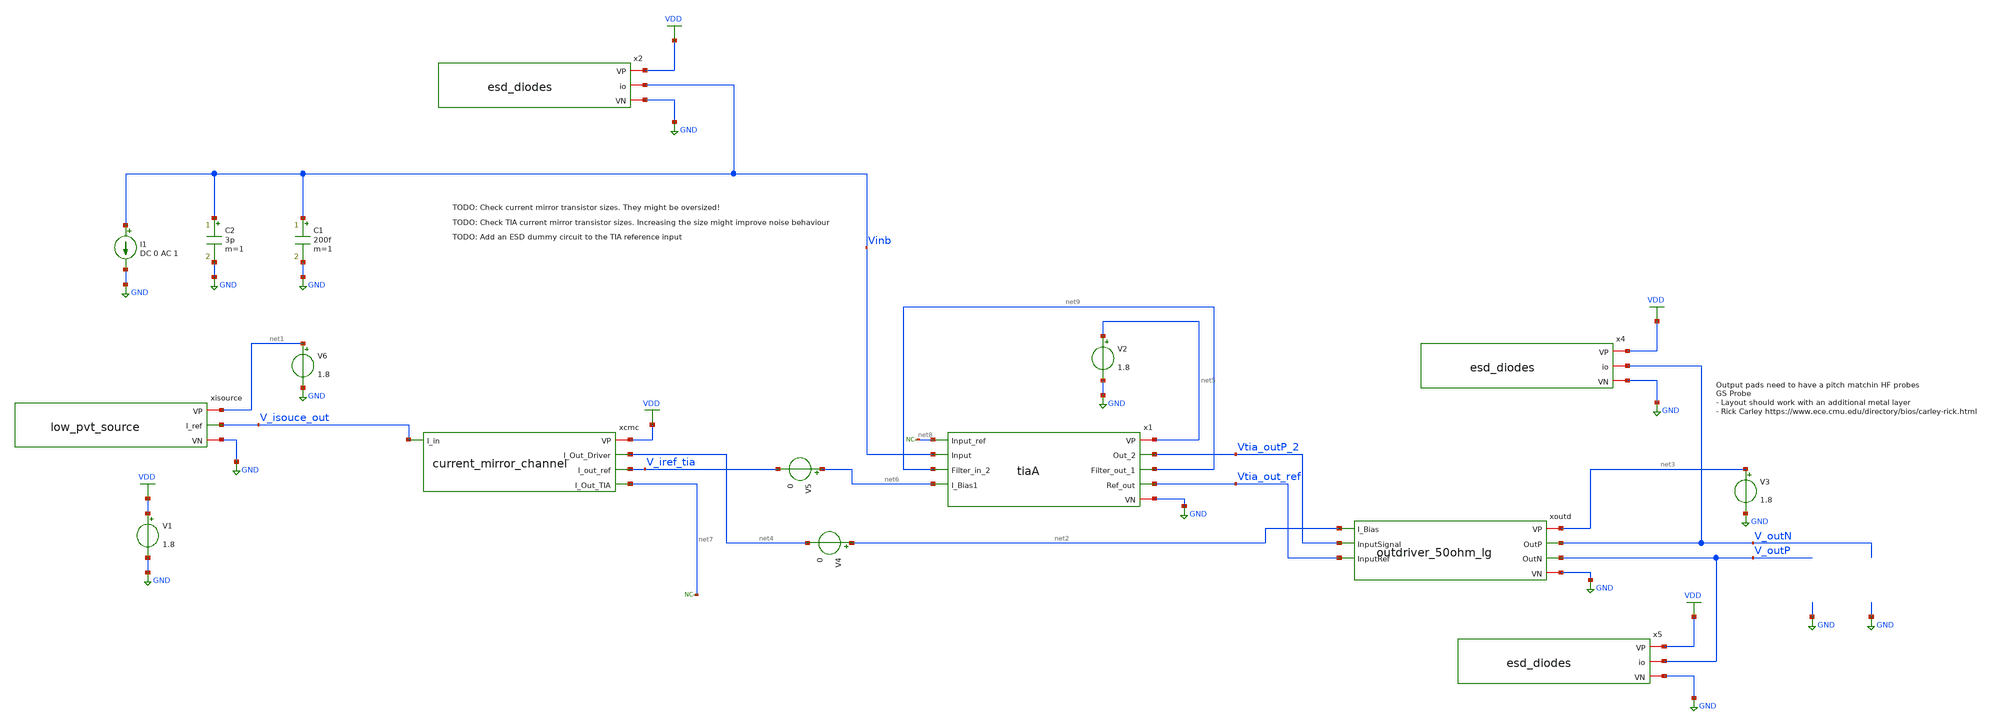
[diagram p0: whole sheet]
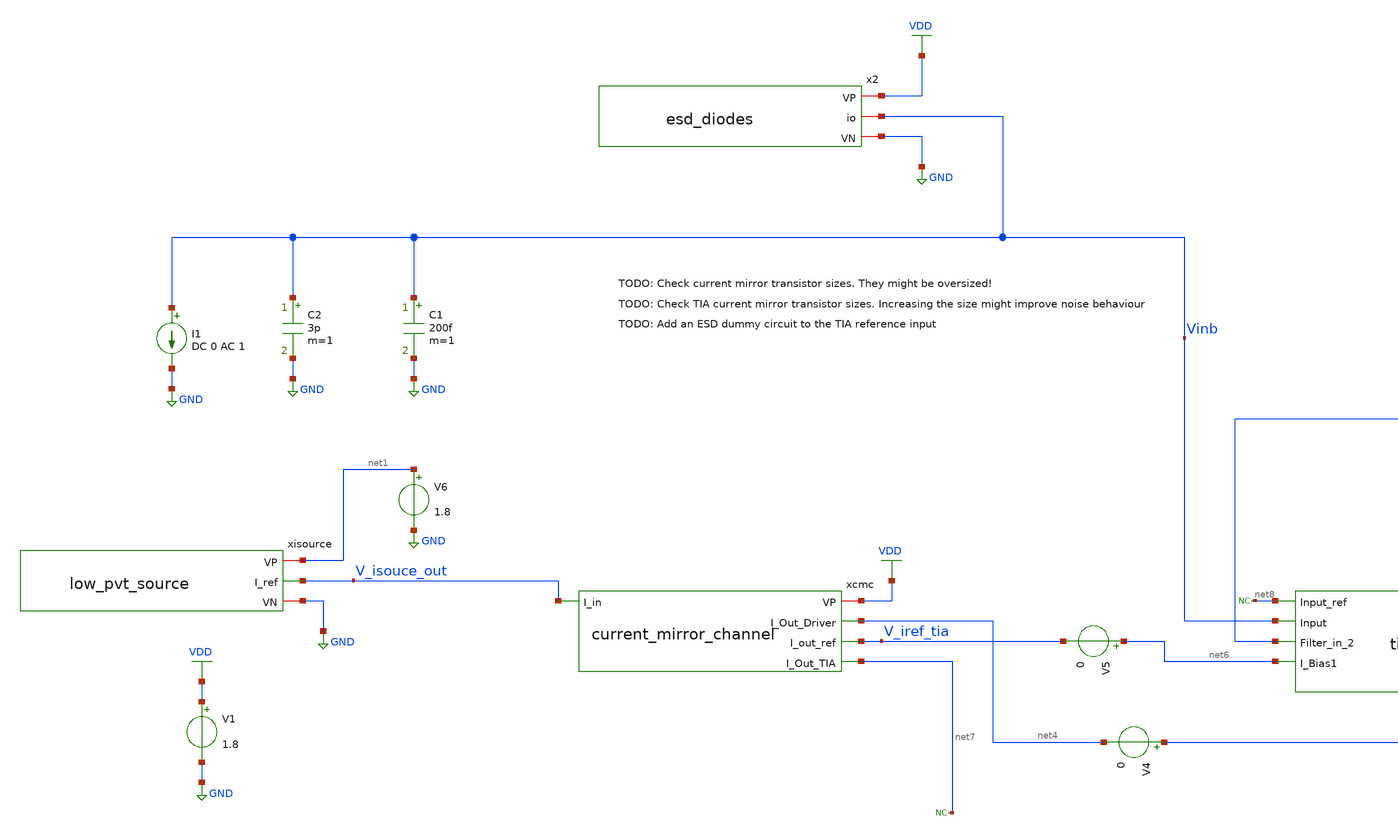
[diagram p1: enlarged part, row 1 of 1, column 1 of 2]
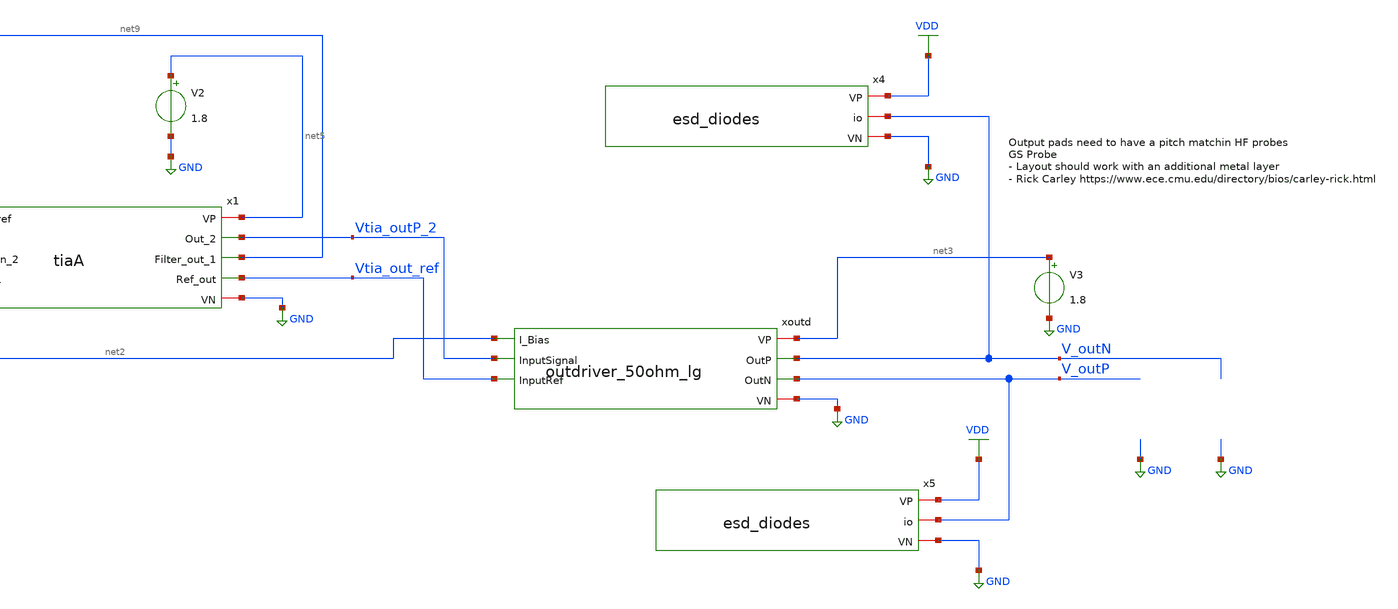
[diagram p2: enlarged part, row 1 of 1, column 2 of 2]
** sch_path: xschem/test/test_tia_integration.sch
**.subckt test_tia_integration
xisource net1 V_isouce_out GND low_pvt_source
V1 VDD GND 1.8
I1 Vinb GND DC 0 AC 1
C1 Vinb GND 200f m=1
C2 Vinb GND 3p m=1
xcmc VDD V_isouce_out net4 V_iref_tia net7 current_mirror_channel
x4 VDD V_outN GND esd_diodes
x5 VDD V_outP GND esd_diodes
x2 VDD Vinb GND esd_diodes
V2 net5 GND 1.8
V3 net3 GND 1.8
V4 net2 net4 0
V5 net6 V_iref_tia 0
V6 net1 GND 1.8
* noconn #net8
* noconn #net7
x1 net5 Vtia_outP_2 net9 net8 Vinb net9 Vtia_out_ref net6 GND tiaA
xoutd net3 V_outN V_outP net2 Vtia_outP_2 Vtia_out_ref GND outdriver_50ohm_lg
**** begin user architecture code


*.options savecurrents
.option warn=1
.option temp=20
.control
set wr_vecnames
set wr_singlescale
set hcopydevtype=svg
** TIA



* save @m.xtia.xm1.msky130_fd_pr__nfet_01v8_lvt[gm]
* save @m.xtia.xm7.msky130_fd_pr__nfet_01v8_lvt[gm]
* save @m.xtia.xm17.msky130_fd_pr__nfet_01v8_lvt[gm]
* save @m.xtia.xm16.msky130_fd_pr__pfet_01v8[gm]
* save @m.xtia.xm8.msky130_fd_pr__pfet_01v8[gm]

* save @m.xtia.xm7.msky130_fd_pr__nfet_01v8_lvt[gm]
* save @m.xtia.xm8.msky130_fd_pr__pfet_01v8[gm]
save all
op
run
write test_tia_integration.raw
reset
save all
ac dec 10 10 1T
plot vdb(Vtia_outP_2)
plot v(Vinb)
plot phase(Vinb)/pi*180 phase(Vtia_outP_1)/pi*180 phase(Vtia_outP_2)/pi*180

*plot phase(Vinb)/pi*180 phase(Vtia_outP_1-Vinb)/pi*180


plot db(v(xoutd.V_da2_P)-v(xoutd.V_da2_N)) - db(v(Vtia_outP_2)-v(Vtia_out_ref))
plot db(v(xoutd.V_da3_P)-v(xoutd.V_da3_N)) - db(v(xoutd.V_da2_P)-v(xoutd.V_da2_N))
plot db(v(xoutd.V_da3_P)-v(xoutd.V_da3_N)) - db(v(Vtia_outP_2)-v(Vtia_out_ref))



*plot db(v(xoutd.V_da2_P)-v(xoutd.V_da2_N)) - db(v(xoutd.V_da1_P)-v(xoutd.V_da1_N))
plot db(v(V_outP)-v(V_outN)) - db(v(xoutd.V_da3_P)-v(xoutd.V_da3_N))


*plot db(v(xoutd.v_da1_P)-v(xoutd.v_da1_N))

plot db(v(V_outP) - v(V_outN))

* tran 1p 100n
* plot v(Vinb)

meas ac gain FIND vdb(vtia_outp_1) AT=10MEG
meas ac max_gain max vdb(vtia_outp_1) from=1MEG to=100G
meas ac min_gain min vdb(vtia_outp_1) from=1MEG to=100MEG
let bw_gain=gain-3
meas ac bandwidth when vdb(vtia_outp_1)=bw_gain fall = LAST
wrdata result_ac_tia.csv gain max_gain min_gain bandwidth


noise v(vtia_outp_2) i1 dec 10 10 2G
print all
* wrdata result_noise.csv inoise_total onoise_total
setplot noise1
plot inoise_spectrum
plot onoise_spectrum
* hardcopy tia_rgc_inoise_spectrum.svg inoise_spectrum
* hardcopy tia_rgc_onoise_spectrum.svg onoise_spectrum
* plot log(inoise_spectrum)
* write noise_tia2.raw

noise v(vtia_outp_2, vtia_out_ref) i1 dec 10 1MEG 2G
print all
* wrdata result_noise.csv inoise_total onoise_total
setplot noise3
plot inoise_spectrum
plot onoise_spectrum
* hardcopy tia_rgc_inoise_spectrum_zoom.svg inoise_spectrum
* hardcopy tia_rgc_onoise_spectrum_zoom.svg onoise_spectrum
* plot log(inoise_spectrum)
* write noise_tia2.raw

noise v(v_outp,v_outn) i1 dec 10 1MEG 2G
print all
setplot noise5
plot inoise_spectrum
plot onoise_spectrum

noise v(v_outp,v_outn) i1 dec 10 10 2G
print all
setplot noise7
plot inoise_spectrum
plot onoise_spectrum


.endc




* .include ../../tia.spice
* .include ../../filter_diff.spice
* .include ../../cmm_sense3.spice

.include tiaA.spice
.include current_mirror_channel.spice
.include low_pvt_source.spice
.include outdriver.spice
.include outdriver_50ohm.spice
.include outdriver_50ohm_lg.spice
.include esd_diodes.spice



* .lib $::SKYWATER_MODELS/sky130.lib.spice #model#
* .lib $::SKYWATER_MODELS/sky130.lib.spice sf
.lib $::SKYWATER_MODELS/sky130.lib.spice.tt.red tt

**** end user architecture code
**.ends

* expanding   symbol:  ../bias/low_pvt_source.sym # of pins=3
** sym_path: ../bias/low_pvt_source.sym
** sch_path: ../bias/low_pvt_source.sch
.subckt low_pvt_source VP I_ref VN
*.iopin VP
*.opin I_ref
*.iopin VN
XM1 VM1D VM8D VP VP sky130_fd_pr__pfet_01v8 L=1 W=4 nf=1 ad='int((nf+1)/2) * W/nf * 0.29' as='int((nf+2)/2) * W/nf * 0.29'
+ pd='2*int((nf+1)/2) * (W/nf + 0.29)' ps='2*int((nf+2)/2) * (W/nf + 0.29)' nrd='0.29 / W' nrs='0.29 / W'
+ sa=0 sb=0 sd=0 mult=10 m=10
XM2 VM2D VM2D VN VN sky130_fd_pr__nfet_01v8 L=6 W=4 nf=1 ad='int((nf+1)/2) * W/nf * 0.29' as='int((nf+2)/2) * W/nf * 0.29'
+ pd='2*int((nf+1)/2) * (W/nf + 0.29)' ps='2*int((nf+2)/2) * (W/nf + 0.29)' nrd='0.29 / W' nrs='0.29 / W'
+ sa=0 sb=0 sd=0 mult=30 m=30
XM5 VM9D VM8D VM1D VP sky130_fd_pr__pfet_01v8 L=0.2 W=4 nf=1 ad='int((nf+1)/2) * W/nf * 0.29' as='int((nf+2)/2) * W/nf * 0.29'
+ pd='2*int((nf+1)/2) * (W/nf + 0.29)' ps='2*int((nf+2)/2) * (W/nf + 0.29)' nrd='0.29 / W' nrs='0.29 / W'
+ sa=0 sb=0 sd=0 mult=2 m=2
XM11 VM11D VM2D VM12D VN sky130_fd_pr__nfet_01v8 L=6 W=4 nf=1 ad='int((nf+1)/2) * W/nf * 0.29' as='int((nf+2)/2) * W/nf * 0.29'
+ pd='2*int((nf+1)/2) * (W/nf + 0.29)' ps='2*int((nf+2)/2) * (W/nf + 0.29)' nrd='0.29 / W' nrs='0.29 / W'
+ sa=0 sb=0 sd=0 mult=65 m=65
XM12 VM12D VM12G VN VN sky130_fd_pr__nfet_01v8 L=6 W=4 nf=1 ad='int((nf+1)/2) * W/nf * 0.29' as='int((nf+2)/2) * W/nf * 0.29'
+ pd='2*int((nf+1)/2) * (W/nf + 0.29)' ps='2*int((nf+2)/2) * (W/nf + 0.29)' nrd='0.29 / W' nrs='0.29 / W'
+ sa=0 sb=0 sd=0 mult=2 m=2
XM14 VM14D VM12G VN VN sky130_fd_pr__nfet_01v8 L=6 W=4 nf=1 ad='int((nf+1)/2) * W/nf * 0.29' as='int((nf+2)/2) * W/nf * 0.29'
+ pd='2*int((nf+1)/2) * (W/nf + 0.29)' ps='2*int((nf+2)/2) * (W/nf + 0.29)' nrd='0.29 / W' nrs='0.29 / W'
+ sa=0 sb=0 sd=0 mult=2 m=2
XM16 VM16D VM8D VP VP sky130_fd_pr__pfet_01v8 L=1 W=4 nf=1 ad='int((nf+1)/2) * W/nf * 0.29' as='int((nf+2)/2) * W/nf * 0.29'
+ pd='2*int((nf+1)/2) * (W/nf + 0.29)' ps='2*int((nf+2)/2) * (W/nf + 0.29)' nrd='0.29 / W' nrs='0.29 / W'
+ sa=0 sb=0 sd=0 mult=10 m=10
XM17 VM8D VM8D VM16D VP sky130_fd_pr__pfet_01v8 L=0.2 W=4 nf=1 ad='int((nf+1)/2) * W/nf * 0.29' as='int((nf+2)/2) * W/nf * 0.29'
+ pd='2*int((nf+1)/2) * (W/nf + 0.29)' ps='2*int((nf+2)/2) * (W/nf + 0.29)' nrd='0.29 / W' nrs='0.29 / W'
+ sa=0 sb=0 sd=0 mult=2 m=2
XM18 VM18D VM8D VP VP sky130_fd_pr__pfet_01v8 L=1 W=4 nf=1 ad='int((nf+1)/2) * W/nf * 0.29' as='int((nf+2)/2) * W/nf * 0.29'
+ pd='2*int((nf+1)/2) * (W/nf + 0.29)' ps='2*int((nf+2)/2) * (W/nf + 0.29)' nrd='0.29 / W' nrs='0.29 / W'
+ sa=0 sb=0 sd=0 mult=10*3*2 m=10*3*2
XM19 VM14D VM8D VM18D VP sky130_fd_pr__pfet_01v8 L=0.2 W=4 nf=1 ad='int((nf+1)/2) * W/nf * 0.29' as='int((nf+2)/2) * W/nf * 0.29'
+ pd='2*int((nf+1)/2) * (W/nf + 0.29)' ps='2*int((nf+2)/2) * (W/nf + 0.29)' nrd='0.29 / W' nrs='0.29 / W'
+ sa=0 sb=0 sd=0 mult=2*3*2 m=2*3*2
XM20 VM20D VM8D VP VP sky130_fd_pr__pfet_01v8 L=1 W=4 nf=1 ad='int((nf+1)/2) * W/nf * 0.29' as='int((nf+2)/2) * W/nf * 0.29'
+ pd='2*int((nf+1)/2) * (W/nf + 0.29)' ps='2*int((nf+2)/2) * (W/nf + 0.29)' nrd='0.29 / W' nrs='0.29 / W'
+ sa=0 sb=0 sd=0 mult=10*1*1 m=10*1*1
XM21 VM22D VM8D VM20D VP sky130_fd_pr__pfet_01v8 L=0.2 W=4 nf=1 ad='int((nf+1)/2) * W/nf * 0.29' as='int((nf+2)/2) * W/nf * 0.29'
+ pd='2*int((nf+1)/2) * (W/nf + 0.29)' ps='2*int((nf+2)/2) * (W/nf + 0.29)' nrd='0.29 / W' nrs='0.29 / W'
+ sa=0 sb=0 sd=0 mult=2*1*1 m=2*1*1
XM22 VM22D VM4S VM3D VN sky130_fd_pr__nfet_01v8 L=6 W=4 nf=1 ad='int((nf+1)/2) * W/nf * 0.29' as='int((nf+2)/2) * W/nf * 0.29'
+ pd='2*int((nf+1)/2) * (W/nf + 0.29)' ps='2*int((nf+2)/2) * (W/nf + 0.29)' nrd='0.29 / W' nrs='0.29 / W'
+ sa=0 sb=0 sd=0 mult=20 m=20
XM3 VM3D VM3G VN VN sky130_fd_pr__nfet_01v8 L=6 W=4 nf=1 ad='int((nf+1)/2) * W/nf * 0.29' as='int((nf+2)/2) * W/nf * 0.29'
+ pd='2*int((nf+1)/2) * (W/nf + 0.29)' ps='2*int((nf+2)/2) * (W/nf + 0.29)' nrd='0.29 / W' nrs='0.29 / W'
+ sa=0 sb=0 sd=0 mult=4 m=4
XM13 VP VM14D VM12G VM12G sky130_fd_pr__nfet_01v8_lvt L=0.15 W=4 nf=1 ad='int((nf+1)/2) * W/nf * 0.29'
+ as='int((nf+2)/2) * W/nf * 0.29' pd='2*int((nf+1)/2) * (W/nf + 0.29)' ps='2*int((nf+2)/2) * (W/nf + 0.29)'
+ nrd='0.29 / W' nrs='0.29 / W' sa=0 sb=0 sd=0 mult=20 m=20
XM4 I_ref VM22D VM4S VN sky130_fd_pr__nfet_01v8_lvt L=0.15 W=4 nf=1 ad='int((nf+1)/2) * W/nf * 0.29'
+ as='int((nf+2)/2) * W/nf * 0.29' pd='2*int((nf+1)/2) * (W/nf + 0.29)' ps='2*int((nf+2)/2) * (W/nf + 0.29)'
+ nrd='0.29 / W' nrs='0.29 / W' sa=0 sb=0 sd=0 mult=20 m=20
XM48 VM50D VM11D VP VP sky130_fd_pr__pfet_01v8 L=2 W=0.5 nf=1 ad='int((nf+1)/2) * W/nf * 0.29' as='int((nf+2)/2) * W/nf * 0.29'
+ pd='2*int((nf+1)/2) * (W/nf + 0.29)' ps='2*int((nf+2)/2) * (W/nf + 0.29)' nrd='0.29 / W' nrs='0.29 / W'
+ sa=0 sb=0 sd=0 mult=1 m=1
XM50 VM50D VM11D VN VN sky130_fd_pr__nfet_01v8_lvt L=0.2 W=4 nf=1 ad='int((nf+1)/2) * W/nf * 0.29' as='int((nf+2)/2) * W/nf * 0.29'
+ pd='2*int((nf+1)/2) * (W/nf + 0.29)' ps='2*int((nf+2)/2) * (W/nf + 0.29)' nrd='0.29 / W' nrs='0.29 / W'
+ sa=0 sb=0 sd=0 mult=10 m=10
XC3 VP VM8D sky130_fd_pr__cap_mim_m3_1 W=20 L=20 MF=1 m=1
XM8 VM8D VM9D VM11D VM11D sky130_fd_pr__nfet_01v8_lvt L=1 W=4 nf=1 ad='int((nf+1)/2) * W/nf * 0.29' as='int((nf+2)/2) * W/nf * 0.29'
+ pd='2*int((nf+1)/2) * (W/nf + 0.29)' ps='2*int((nf+2)/2) * (W/nf + 0.29)' nrd='0.29 / W' nrs='0.29 / W'
+ sa=0 sb=0 sd=0 mult=20 m=20
XM9 VM9D VM9D VM2D VM2D sky130_fd_pr__nfet_01v8_lvt L=1 W=4 nf=1 ad='int((nf+1)/2) * W/nf * 0.29' as='int((nf+2)/2) * W/nf * 0.29'
+ pd='2*int((nf+1)/2) * (W/nf + 0.29)' ps='2*int((nf+2)/2) * (W/nf + 0.29)' nrd='0.29 / W' nrs='0.29 / W'
+ sa=0 sb=0 sd=0 mult=20 m=20
XM10 VM8D VM50D VN VN sky130_fd_pr__nfet_01v8 L=2 W=0.5 nf=1 ad='int((nf+1)/2) * W/nf * 0.29' as='int((nf+2)/2) * W/nf * 0.29'
+ pd='2*int((nf+1)/2) * (W/nf + 0.29)' ps='2*int((nf+2)/2) * (W/nf + 0.29)' nrd='0.29 / W' nrs='0.29 / W'
+ sa=0 sb=0 sd=0 mult=1 m=1
XR7 net3 VM4S VN sky130_fd_pr__res_xhigh_po_1p41 L=10 mult=1 m=1
XR3 net4 net3 VN sky130_fd_pr__res_xhigh_po_1p41 L=10 mult=1 m=1
XR4 net2 net4 VN sky130_fd_pr__res_xhigh_po_1p41 L=10 mult=1 m=1
XR5 net1 net2 VN sky130_fd_pr__res_xhigh_po_1p41 L=10 mult=1 m=1
XR6 VN net1 VN sky130_fd_pr__res_xhigh_po_1p41 L=10 mult=1 m=1
XR8 net5 VM12G VN sky130_fd_pr__res_xhigh_po_1p41 L=10 mult=1 m=1
XR1 net5 VM3G VN sky130_fd_pr__res_xhigh_po_1p41 L=10 mult=1 m=1
XR2 net7 net6 VN sky130_fd_pr__res_xhigh_po_1p41 L=10 mult=1 m=1
XR9 VN net6 VN sky130_fd_pr__res_xhigh_po_1p41 L=10 mult=1 m=1
XR10 net11 net7 VN sky130_fd_pr__res_xhigh_po_1p41 L=10 mult=1 m=1
XR11 net12 net11 VN sky130_fd_pr__res_xhigh_po_1p41 L=10 mult=1 m=1
XR12 net8 net12 VN sky130_fd_pr__res_xhigh_po_1p41 L=10 mult=1 m=1
XR13 net10 VM3G VN sky130_fd_pr__res_xhigh_po_1p41 L=10 mult=1 m=1
XR14 net9 net10 VN sky130_fd_pr__res_xhigh_po_1p41 L=10 mult=1 m=1
XR15 net8 net9 VN sky130_fd_pr__res_xhigh_po_1p41 L=10 mult=1 m=1
XC2 VP VN sky130_fd_pr__cap_mim_m3_1 W=25 L=30 MF=1 m=1
XC1 VP VN sky130_fd_pr__cap_mim_m3_1 W=25 L=30 MF=1 m=1
.ends


* expanding   symbol:  ../bias/current_mirror_channel.sym # of pins=5
** sym_path: xschem/bias/current_mirror_channel.sym
** sch_path: xschem/bias/current_mirror_channel.sch
.subckt current_mirror_channel VP I_in I_Out_Driver I_out_ref I_Out_TIA
*.ipin I_in
*.iopin VP
*.opin I_Out_TIA
*.opin I_Out_Driver
*.opin I_out_ref
XM13 VM13D I_in VP VP sky130_fd_pr__pfet_01v8 L=1 W=2 nf=1 ad='int((nf+1)/2) * W/nf * 0.29' as='int((nf+2)/2) * W/nf * 0.29'
+ pd='2*int((nf+1)/2) * (W/nf + 0.29)' ps='2*int((nf+2)/2) * (W/nf + 0.29)' nrd='0.29 / W' nrs='0.29 / W'
+ sa=0 sb=0 sd=0 mult=8*16 m=8*16
XM11 VM11D I_in VP VP sky130_fd_pr__pfet_01v8 L=1 W=2 nf=1 ad='int((nf+1)/2) * W/nf * 0.29' as='int((nf+2)/2) * W/nf * 0.29'
+ pd='2*int((nf+1)/2) * (W/nf + 0.29)' ps='2*int((nf+2)/2) * (W/nf + 0.29)' nrd='0.29 / W' nrs='0.29 / W'
+ sa=0 sb=0 sd=0 mult=16 m=16
XM2 I_in I_in VM11D VP sky130_fd_pr__pfet_01v8 L=0.15 W=2 nf=1 ad='int((nf+1)/2) * W/nf * 0.29' as='int((nf+2)/2) * W/nf * 0.29'
+ pd='2*int((nf+1)/2) * (W/nf + 0.29)' ps='2*int((nf+2)/2) * (W/nf + 0.29)' nrd='0.29 / W' nrs='0.29 / W'
+ sa=0 sb=0 sd=0 mult=16 m=16
XM4 I_Out_TIA I_in VM13D VP sky130_fd_pr__pfet_01v8 L=0.15 W=2 nf=1 ad='int((nf+1)/2) * W/nf * 0.29'
+ as='int((nf+2)/2) * W/nf * 0.29' pd='2*int((nf+1)/2) * (W/nf + 0.29)' ps='2*int((nf+2)/2) * (W/nf + 0.29)'
+ nrd='0.29 / W' nrs='0.29 / W' sa=0 sb=0 sd=0 mult=8*16 m=8*16
XM1 VM1D I_in VP VP sky130_fd_pr__pfet_01v8 L=1 W=2 nf=1 ad='int((nf+1)/2) * W/nf * 0.29' as='int((nf+2)/2) * W/nf * 0.29'
+ pd='2*int((nf+1)/2) * (W/nf + 0.29)' ps='2*int((nf+2)/2) * (W/nf + 0.29)' nrd='0.29 / W' nrs='0.29 / W'
+ sa=0 sb=0 sd=0 mult=2*2*8*16 m=2*2*8*16
XM3 I_Out_Driver I_in VM1D VP sky130_fd_pr__pfet_01v8 L=0.15 W=2 nf=1 ad='int((nf+1)/2) * W/nf * 0.29'
+ as='int((nf+2)/2) * W/nf * 0.29' pd='2*int((nf+1)/2) * (W/nf + 0.29)' ps='2*int((nf+2)/2) * (W/nf + 0.29)'
+ nrd='0.29 / W' nrs='0.29 / W' sa=0 sb=0 sd=0 mult=2*2*8*16 m=2*2*8*16
XM5 VM5D I_in VP VP sky130_fd_pr__pfet_01v8 L=1 W=2 nf=1 ad='int((nf+1)/2) * W/nf * 0.29' as='int((nf+2)/2) * W/nf * 0.29'
+ pd='2*int((nf+1)/2) * (W/nf + 0.29)' ps='2*int((nf+2)/2) * (W/nf + 0.29)' nrd='0.29 / W' nrs='0.29 / W'
+ sa=0 sb=0 sd=0 mult=8*16 m=8*16
XM6 I_out_ref I_in VM5D VP sky130_fd_pr__pfet_01v8 L=0.15 W=2 nf=1 ad='int((nf+1)/2) * W/nf * 0.29' as='int((nf+2)/2) * W/nf * 0.29'
+ pd='2*int((nf+1)/2) * (W/nf + 0.29)' ps='2*int((nf+2)/2) * (W/nf + 0.29)' nrd='0.29 / W' nrs='0.29 / W'
+ sa=0 sb=0 sd=0 mult=8*16 m=8*16
.ends


* expanding   symbol:  ../esd/esd_diodes.sym # of pins=3
** sym_path: ../esd/esd_diodes.sym
** sch_path: ../esd/esd_diodes.sch
.subckt esd_diodes VP io VN
*.iopin VP
*.iopin io
*.iopin VN
XD1 io VP sky130_fd_pr__diode_pw2nd_05v5 area=4e12 pj=4e6
XD2 io VP sky130_fd_pr__diode_pw2nd_05v5 area=4e12 pj=4e6
XD3 io VP sky130_fd_pr__diode_pw2nd_05v5 area=4e12 pj=4e6
XD4 io VP sky130_fd_pr__diode_pw2nd_05v5 area=4e12 pj=4e6
XD5 io VP sky130_fd_pr__diode_pw2nd_05v5 area=4e12 pj=4e6
XD6 io VP sky130_fd_pr__diode_pw2nd_05v5 area=4e12 pj=4e6
XD7 io VP sky130_fd_pr__diode_pw2nd_05v5 area=4e12 pj=4e6
XD8 io VP sky130_fd_pr__diode_pw2nd_05v5 area=4e12 pj=4e6
XD9 io VP sky130_fd_pr__diode_pw2nd_05v5 area=4e12 pj=4e6
XD10 io VP sky130_fd_pr__diode_pw2nd_05v5 area=4e12 pj=4e6
XD11 VN io sky130_fd_pr__diode_pw2nd_05v5 area=4e12 pj=4e6
XD12 VN io sky130_fd_pr__diode_pw2nd_05v5 area=4e12 pj=4e6
XD13 VN io sky130_fd_pr__diode_pw2nd_05v5 area=4e12 pj=4e6
XD14 VN io sky130_fd_pr__diode_pw2nd_05v5 area=4e12 pj=4e6
XD15 VN io sky130_fd_pr__diode_pw2nd_05v5 area=4e12 pj=4e6
XD16 VN io sky130_fd_pr__diode_pw2nd_05v5 area=4e12 pj=4e6
XD17 VN io sky130_fd_pr__diode_pw2nd_05v5 area=4e12 pj=4e6
XD18 VN io sky130_fd_pr__diode_pw2nd_05v5 area=4e12 pj=4e6
XD19 VN io sky130_fd_pr__diode_pw2nd_05v5 area=4e12 pj=4e6
XD20 VN io sky130_fd_pr__diode_pw2nd_05v5 area=4e12 pj=4e6
.ends


* expanding   symbol:  /home/simon/code/hibpm-sky130a-tapeout/xschem/tia/tiaA.sym # of pins=9
** sym_path: xschem/tia/tiaA.sym
** sch_path: xschem/tia/tiaA.sch
.subckt tiaA VP Out_2 Filter_out_1 Input_ref Input Filter_in_2 Ref_out I_Bias1 VN
*.iopin VN
*.iopin VP
*.opin Out_2
*.ipin I_Bias1
*.ipin Input
*.ipin Input_ref
*.opin Filter_out_1
*.ipin Filter_in_2
*.opin Ref_out
XM7 VM7D Input VN VN sky130_fd_pr__nfet_01v8_lvt L=0.15 W=2 nf=1 ad='int((nf+1)/2) * W/nf * 0.29' as='int((nf+2)/2) * W/nf * 0.29'
+ pd='2*int((nf+1)/2) * (W/nf + 0.29)' ps='2*int((nf+2)/2) * (W/nf + 0.29)' nrd='0.29 / W' nrs='0.29 / W'
+ sa=0 sb=0 sd=0 mult=180 m=180
XM8 net1 Input VP VP sky130_fd_pr__pfet_01v8 L=0.15 W=2 nf=1 ad='int((nf+1)/2) * W/nf * 0.29' as='int((nf+2)/2) * W/nf * 0.29'
+ pd='2*int((nf+1)/2) * (W/nf + 0.29)' ps='2*int((nf+2)/2) * (W/nf + 0.29)' nrd='0.29 / W' nrs='0.29 / W'
+ sa=0 sb=0 sd=0 mult=40 m=40
XC4 VN VM9G sky130_fd_pr__cap_mim_m3_1 W=15 L=20 MF=1 m=1
XM18 I_Bias1 I_Bias1 VM10G VN sky130_fd_pr__nfet_01v8_lvt L=0.15 W=2 nf=1 ad='int((nf+1)/2) * W/nf * 0.29'
+ as='int((nf+2)/2) * W/nf * 0.29' pd='2*int((nf+1)/2) * (W/nf + 0.29)' ps='2*int((nf+2)/2) * (W/nf + 0.29)'
+ nrd='0.29 / W' nrs='0.29 / W' sa=0 sb=0 sd=0 mult=30 m=30
XM10 VM10G VM10G VM6D VN sky130_fd_pr__nfet_01v8_lvt L=0.15 W=2 nf=1 ad='int((nf+1)/2) * W/nf * 0.29'
+ as='int((nf+2)/2) * W/nf * 0.29' pd='2*int((nf+1)/2) * (W/nf + 0.29)' ps='2*int((nf+2)/2) * (W/nf + 0.29)'
+ nrd='0.29 / W' nrs='0.29 / W' sa=0 sb=0 sd=0 mult=30 m=30
XM5 Input VM9G VM5D VN sky130_fd_pr__nfet_01v8_lvt L=0.15 W=2 nf=1 ad='int((nf+1)/2) * W/nf * 0.29' as='int((nf+2)/2) * W/nf * 0.29'
+ pd='2*int((nf+1)/2) * (W/nf + 0.29)' ps='2*int((nf+2)/2) * (W/nf + 0.29)' nrd='0.29 / W' nrs='0.29 / W'
+ sa=0 sb=0 sd=0 mult=120 m=120
XM6 VM6D VM10G VN VN sky130_fd_pr__nfet_01v8_lvt L=1 W=2 nf=1 ad='int((nf+1)/2) * W/nf * 0.29' as='int((nf+2)/2) * W/nf * 0.29'
+ pd='2*int((nf+1)/2) * (W/nf + 0.29)' ps='2*int((nf+2)/2) * (W/nf + 0.29)' nrd='0.29 / W' nrs='0.29 / W'
+ sa=0 sb=0 sd=0 mult=30 m=30
XM14 VM9G I_Bias1 VM10G VN sky130_fd_pr__nfet_01v8_lvt L=8 W=1 nf=1 ad='int((nf+1)/2) * W/nf * 0.29'
+ as='int((nf+2)/2) * W/nf * 0.29' pd='2*int((nf+1)/2) * (W/nf + 0.29)' ps='2*int((nf+2)/2) * (W/nf + 0.29)'
+ nrd='0.29 / W' nrs='0.29 / W' sa=0 sb=0 sd=0 mult=1 m=1
XM1 Out_2 net1 Input Input sky130_fd_pr__nfet_01v8_lvt L=0.15 W=2 nf=1 ad='int((nf+1)/2) * W/nf * 0.29'
+ as='int((nf+2)/2) * W/nf * 0.29' pd='2*int((nf+1)/2) * (W/nf + 0.29)' ps='2*int((nf+2)/2) * (W/nf + 0.29)'
+ nrd='0.29 / W' nrs='0.29 / W' sa=0 sb=0 sd=0 mult=60 m=60
XM3 VM5D VM9G VN VN sky130_fd_pr__nfet_01v8_lvt L=1 W=2 nf=1 ad='int((nf+1)/2) * W/nf * 0.29' as='int((nf+2)/2) * W/nf * 0.29'
+ pd='2*int((nf+1)/2) * (W/nf + 0.29)' ps='2*int((nf+2)/2) * (W/nf + 0.29)' nrd='0.29 / W' nrs='0.29 / W'
+ sa=0 sb=0 sd=0 mult=120 m=120
XR1 Out_2 VP VN sky130_fd_pr__res_xhigh_po_1p41 L=4 mult=6 m=6
XM2 VM2D Input_ref VN VN sky130_fd_pr__nfet_01v8_lvt L=0.15 W=2 nf=1 ad='int((nf+1)/2) * W/nf * 0.29'
+ as='int((nf+2)/2) * W/nf * 0.29' pd='2*int((nf+1)/2) * (W/nf + 0.29)' ps='2*int((nf+2)/2) * (W/nf + 0.29)'
+ nrd='0.29 / W' nrs='0.29 / W' sa=0 sb=0 sd=0 mult=180 m=180
XM4 net3 Input_ref VP VP sky130_fd_pr__pfet_01v8 L=0.15 W=2 nf=1 ad='int((nf+1)/2) * W/nf * 0.29' as='int((nf+2)/2) * W/nf * 0.29'
+ pd='2*int((nf+1)/2) * (W/nf + 0.29)' ps='2*int((nf+2)/2) * (W/nf + 0.29)' nrd='0.29 / W' nrs='0.29 / W'
+ sa=0 sb=0 sd=0 mult=40 m=40
XM11 Input_ref VM9G VM15D VN sky130_fd_pr__nfet_01v8_lvt L=0.15 W=2 nf=1 ad='int((nf+1)/2) * W/nf * 0.29'
+ as='int((nf+2)/2) * W/nf * 0.29' pd='2*int((nf+1)/2) * (W/nf + 0.29)' ps='2*int((nf+2)/2) * (W/nf + 0.29)'
+ nrd='0.29 / W' nrs='0.29 / W' sa=0 sb=0 sd=0 mult=120 m=120
XM12 net2 net3 Input_ref Input_ref sky130_fd_pr__nfet_01v8_lvt L=0.15 W=2 nf=1 ad='int((nf+1)/2) * W/nf * 0.29'
+ as='int((nf+2)/2) * W/nf * 0.29' pd='2*int((nf+1)/2) * (W/nf + 0.29)' ps='2*int((nf+2)/2) * (W/nf + 0.29)'
+ nrd='0.29 / W' nrs='0.29 / W' sa=0 sb=0 sd=0 mult=60 m=60
XM15 VM15D VM9G VN VN sky130_fd_pr__nfet_01v8_lvt L=1 W=2 nf=1 ad='int((nf+1)/2) * W/nf * 0.29' as='int((nf+2)/2) * W/nf * 0.29'
+ pd='2*int((nf+1)/2) * (W/nf + 0.29)' ps='2*int((nf+2)/2) * (W/nf + 0.29)' nrd='0.29 / W' nrs='0.29 / W'
+ sa=0 sb=0 sd=0 mult=120 m=120
XR2 net2 VP VN sky130_fd_pr__res_xhigh_po_1p41 L=4 mult=6 m=6
XC5 VN VP sky130_fd_pr__cap_mim_m3_1 W=15 L=30 MF=1 m=1
XC1 VN VP sky130_fd_pr__cap_mim_m3_1 W=15 L=30 MF=1 m=1
XC2 VN Filter_out_1 sky130_fd_pr__cap_mim_m3_1 W=30 L=10 MF=1 m=1
XM29 VM29D VM9G VM33D VN sky130_fd_pr__nfet_01v8_lvt L=0.15 W=2 nf=1 ad='int((nf+1)/2) * W/nf * 0.29'
+ as='int((nf+2)/2) * W/nf * 0.29' pd='2*int((nf+1)/2) * (W/nf + 0.29)' ps='2*int((nf+2)/2) * (W/nf + 0.29)'
+ nrd='0.29 / W' nrs='0.29 / W' sa=0 sb=0 sd=0 mult=20 m=20
XM33 VM33D VM9G VN VN sky130_fd_pr__nfet_01v8_lvt L=1 W=2 nf=1 ad='int((nf+1)/2) * W/nf * 0.29' as='int((nf+2)/2) * W/nf * 0.29'
+ pd='2*int((nf+1)/2) * (W/nf + 0.29)' ps='2*int((nf+2)/2) * (W/nf + 0.29)' nrd='0.29 / W' nrs='0.29 / W'
+ sa=0 sb=0 sd=0 mult=20 m=20
XR3 VM21D VP VN sky130_fd_pr__res_xhigh_po_1p41 L=4 mult=1 m=1
XM21 VM29D VM29D VM21D VP sky130_fd_pr__pfet_01v8 L=0.15 W=2 nf=1 ad='int((nf+1)/2) * W/nf * 0.29' as='int((nf+2)/2) * W/nf * 0.29'
+ pd='2*int((nf+1)/2) * (W/nf + 0.29)' ps='2*int((nf+2)/2) * (W/nf + 0.29)' nrd='0.29 / W' nrs='0.29 / W'
+ sa=0 sb=0 sd=0 mult=10 m=10
XM13 Filter_out_1 VM29D net2 VP sky130_fd_pr__pfet_01v8 L=8 W=1 nf=1 ad='int((nf+1)/2) * W/nf * 0.29'
+ as='int((nf+2)/2) * W/nf * 0.29' pd='2*int((nf+1)/2) * (W/nf + 0.29)' ps='2*int((nf+2)/2) * (W/nf + 0.29)'
+ nrd='0.29 / W' nrs='0.29 / W' sa=0 sb=0 sd=0 mult=1 m=1
XM24 VM24D Input_ref VN VN sky130_fd_pr__nfet_01v8_lvt L=0.15 W=2 nf=1 ad='int((nf+1)/2) * W/nf * 0.29'
+ as='int((nf+2)/2) * W/nf * 0.29' pd='2*int((nf+1)/2) * (W/nf + 0.29)' ps='2*int((nf+2)/2) * (W/nf + 0.29)'
+ nrd='0.29 / W' nrs='0.29 / W' sa=0 sb=0 sd=0 mult=20 m=20
XM30 VM30D VM9G VM31D VN sky130_fd_pr__nfet_01v8_lvt L=0.15 W=2 nf=1 ad='int((nf+1)/2) * W/nf * 0.29'
+ as='int((nf+2)/2) * W/nf * 0.29' pd='2*int((nf+1)/2) * (W/nf + 0.29)' ps='2*int((nf+2)/2) * (W/nf + 0.29)'
+ nrd='0.29 / W' nrs='0.29 / W' sa=0 sb=0 sd=0 mult=2*30 m=2*30
XM31 VM31D VM9G VN VN sky130_fd_pr__nfet_01v8_lvt L=1 W=2 nf=1 ad='int((nf+1)/2) * W/nf * 0.29' as='int((nf+2)/2) * W/nf * 0.29'
+ pd='2*int((nf+1)/2) * (W/nf + 0.29)' ps='2*int((nf+2)/2) * (W/nf + 0.29)' nrd='0.29 / W' nrs='0.29 / W'
+ sa=0 sb=0 sd=0 mult=2*30 m=2*30
XM28 VM28D VM28D VM24D VN sky130_fd_pr__nfet_01v8_lvt L=0.15 W=2 nf=1 ad='int((nf+1)/2) * W/nf * 0.29'
+ as='int((nf+2)/2) * W/nf * 0.29' pd='2*int((nf+1)/2) * (W/nf + 0.29)' ps='2*int((nf+2)/2) * (W/nf + 0.29)'
+ nrd='0.29 / W' nrs='0.29 / W' sa=0 sb=0 sd=0 mult=7 m=7
XM17 net1 VM28D VM7D VN sky130_fd_pr__nfet_01v8_lvt L=0.15 W=2 nf=1 ad='int((nf+1)/2) * W/nf * 0.29'
+ as='int((nf+2)/2) * W/nf * 0.29' pd='2*int((nf+1)/2) * (W/nf + 0.29)' ps='2*int((nf+2)/2) * (W/nf + 0.29)'
+ nrd='0.29 / W' nrs='0.29 / W' sa=0 sb=0 sd=0 mult=40 m=40
XM9 net3 VM28D VM2D VN sky130_fd_pr__nfet_01v8_lvt L=0.15 W=2 nf=1 ad='int((nf+1)/2) * W/nf * 0.29' as='int((nf+2)/2) * W/nf * 0.29'
+ pd='2*int((nf+1)/2) * (W/nf + 0.29)' ps='2*int((nf+2)/2) * (W/nf + 0.29)' nrd='0.29 / W' nrs='0.29 / W'
+ sa=0 sb=0 sd=0 mult=40 m=40
XC10 VN VM28D sky130_fd_pr__cap_mim_m3_1 W=25 L=10 MF=1 m=1
XC11 VN VM28D sky130_fd_pr__cap_mim_m3_1 W=25 L=10 MF=1 m=1
XM36 VM36D VM30D VP VP sky130_fd_pr__pfet_01v8 L=0.5 W=2 nf=1 ad='int((nf+1)/2) * W/nf * 0.29' as='int((nf+2)/2) * W/nf * 0.29'
+ pd='2*int((nf+1)/2) * (W/nf + 0.29)' ps='2*int((nf+2)/2) * (W/nf + 0.29)' nrd='0.29 / W' nrs='0.29 / W'
+ sa=0 sb=0 sd=0 mult=1*30 m=1*30
XM16 VM16D VM30D VP VP sky130_fd_pr__pfet_01v8 L=0.5 W=2 nf=1 ad='int((nf+1)/2) * W/nf * 0.29' as='int((nf+2)/2) * W/nf * 0.29'
+ pd='2*int((nf+1)/2) * (W/nf + 0.29)' ps='2*int((nf+2)/2) * (W/nf + 0.29)' nrd='0.29 / W' nrs='0.29 / W'
+ sa=0 sb=0 sd=0 mult=4*30 m=4*30
XM19 VM28D VM30D VM16D VP sky130_fd_pr__pfet_01v8 L=0.15 W=2 nf=1 ad='int((nf+1)/2) * W/nf * 0.29' as='int((nf+2)/2) * W/nf * 0.29'
+ pd='2*int((nf+1)/2) * (W/nf + 0.29)' ps='2*int((nf+2)/2) * (W/nf + 0.29)' nrd='0.29 / W' nrs='0.29 / W'
+ sa=0 sb=0 sd=0 mult=4*30 m=4*30
XM20 VM30D VM30D VM36D VP sky130_fd_pr__pfet_01v8 L=0.15 W=2 nf=1 ad='int((nf+1)/2) * W/nf * 0.29' as='int((nf+2)/2) * W/nf * 0.29'
+ pd='2*int((nf+1)/2) * (W/nf + 0.29)' ps='2*int((nf+2)/2) * (W/nf + 0.29)' nrd='0.29 / W' nrs='0.29 / W'
+ sa=0 sb=0 sd=0 mult=1*30 m=1*30
XC8 VN Ref_out sky130_fd_pr__cap_mim_m3_1 W=5 L=2 MF=1 m=1
XR9 Ref_out Filter_in_2 VN sky130_fd_pr__res_xhigh_po_0p69 L=6 mult=1 m=1
XC3 VN VM9G sky130_fd_pr__cap_mim_m3_1 W=15 L=20 MF=1 m=1
.ends


* expanding   symbol:
*+  /home/simon/code/hibpm-sky130a-tapeout/xschem/outdriver/outdriver_50ohm_lg.sym # of pins=7
** sym_path: xschem/outdriver/outdriver_50ohm_lg.sym
** sch_path: xschem/outdriver/outdriver_50ohm_lg.sch
.subckt outdriver_50ohm_lg VP OutP OutN I_Bias InputSignal InputRef VN
*.iopin VN
*.ipin InputRef
*.iopin VP
*.ipin I_Bias
*.ipin InputSignal
*.opin OutN
*.opin OutP
XM17 net1 VM18D VN VN sky130_fd_pr__nfet_01v8_lvt L=0.3 W=2 nf=1 ad='int((nf+1)/2) * W/nf * 0.29' as='int((nf+2)/2) * W/nf * 0.29'
+ pd='2*int((nf+1)/2) * (W/nf + 0.29)' ps='2*int((nf+2)/2) * (W/nf + 0.29)' nrd='0.29 / W' nrs='0.29 / W'
+ sa=0 sb=0 sd=0 mult=6 m=6
XM18 VM18D VM18D net1 VN sky130_fd_pr__nfet_01v8_lvt L=0.15 W=2 nf=1 ad='int((nf+1)/2) * W/nf * 0.29'
+ as='int((nf+2)/2) * W/nf * 0.29' pd='2*int((nf+1)/2) * (W/nf + 0.29)' ps='2*int((nf+2)/2) * (W/nf + 0.29)'
+ nrd='0.29 / W' nrs='0.29 / W' sa=0 sb=0 sd=0 mult=12 m=12
XM7 I_Bias I_Bias VM18D VM18D sky130_fd_pr__nfet_01v8_lvt L=0.15 W=2 nf=1 ad='int((nf+1)/2) * W/nf * 0.29'
+ as='int((nf+2)/2) * W/nf * 0.29' pd='2*int((nf+1)/2) * (W/nf + 0.29)' ps='2*int((nf+2)/2) * (W/nf + 0.29)'
+ nrd='0.29 / W' nrs='0.29 / W' sa=0 sb=0 sd=0 mult=20 m=20
XM5 VM5D net2 net3 VN sky130_fd_pr__nfet_01v8_lvt L=0.15 W=2 nf=1 ad='int((nf+1)/2) * W/nf * 0.29' as='int((nf+2)/2) * W/nf * 0.29'
+ pd='2*int((nf+1)/2) * (W/nf + 0.29)' ps='2*int((nf+2)/2) * (W/nf + 0.29)' nrd='0.29 / W' nrs='0.29 / W'
+ sa=0 sb=0 sd=0 mult=12*5 m=12*5
XM8 net3 net2 VN VN sky130_fd_pr__nfet_01v8_lvt L=0.3 W=2 nf=1 ad='int((nf+1)/2) * W/nf * 0.29' as='int((nf+2)/2) * W/nf * 0.29'
+ pd='2*int((nf+1)/2) * (W/nf + 0.29)' ps='2*int((nf+2)/2) * (W/nf + 0.29)' nrd='0.29 / W' nrs='0.29 / W'
+ sa=0 sb=0 sd=0 mult=6*5 m=6*5
XM6 net2 I_Bias VM18D VM18D sky130_fd_pr__nfet_01v8_lvt L=8 W=1 nf=1 ad='int((nf+1)/2) * W/nf * 0.29'
+ as='int((nf+2)/2) * W/nf * 0.29' pd='2*int((nf+1)/2) * (W/nf + 0.29)' ps='2*int((nf+2)/2) * (W/nf + 0.29)'
+ nrd='0.29 / W' nrs='0.29 / W' sa=0 sb=0 sd=0 mult=1 m=1
XC1 VN VP sky130_fd_pr__cap_mim_m3_1 W=15 L=30 MF=1 m=1
XM15 VM15D net2 net4 VN sky130_fd_pr__nfet_01v8_lvt L=0.15 W=2 nf=1 ad='int((nf+1)/2) * W/nf * 0.29'
+ as='int((nf+2)/2) * W/nf * 0.29' pd='2*int((nf+1)/2) * (W/nf + 0.29)' ps='2*int((nf+2)/2) * (W/nf + 0.29)'
+ nrd='0.29 / W' nrs='0.29 / W' sa=0 sb=0 sd=0 mult=34*12 m=34*12
XM16 net4 net2 VN VN sky130_fd_pr__nfet_01v8_lvt L=0.3 W=2 nf=1 ad='int((nf+1)/2) * W/nf * 0.29' as='int((nf+2)/2) * W/nf * 0.29'
+ pd='2*int((nf+1)/2) * (W/nf + 0.29)' ps='2*int((nf+2)/2) * (W/nf + 0.29)' nrd='0.29 / W' nrs='0.29 / W'
+ sa=0 sb=0 sd=0 mult=34*6 m=34*6
XM4 OutP V_da2_N VM15D VN sky130_fd_pr__nfet_01v8_lvt L=0.15 W=2 nf=1 ad='int((nf+1)/2) * W/nf * 0.29'
+ as='int((nf+2)/2) * W/nf * 0.29' pd='2*int((nf+1)/2) * (W/nf + 0.29)' ps='2*int((nf+2)/2) * (W/nf + 0.29)'
+ nrd='0.29 / W' nrs='0.29 / W' sa=0 sb=0 sd=0 mult=30 m=30
XM23 V_da2_P InputSignal VM5D VN sky130_fd_pr__nfet_01v8_lvt L=0.15 W=2 nf=1 ad='int((nf+1)/2) * W/nf * 0.29'
+ as='int((nf+2)/2) * W/nf * 0.29' pd='2*int((nf+1)/2) * (W/nf + 0.29)' ps='2*int((nf+2)/2) * (W/nf + 0.29)'
+ nrd='0.29 / W' nrs='0.29 / W' sa=0 sb=0 sd=0 mult=6 m=6
XM19 OutN V_da2_P VM15D VN sky130_fd_pr__nfet_01v8_lvt L=0.15 W=2 nf=1 ad='int((nf+1)/2) * W/nf * 0.29'
+ as='int((nf+2)/2) * W/nf * 0.29' pd='2*int((nf+1)/2) * (W/nf + 0.29)' ps='2*int((nf+2)/2) * (W/nf + 0.29)'
+ nrd='0.29 / W' nrs='0.29 / W' sa=0 sb=0 sd=0 mult=30 m=30
XM14 V_da2_N InputRef VM5D VN sky130_fd_pr__nfet_01v8_lvt L=0.15 W=2 nf=1 ad='int((nf+1)/2) * W/nf * 0.29'
+ as='int((nf+2)/2) * W/nf * 0.29' pd='2*int((nf+1)/2) * (W/nf + 0.29)' ps='2*int((nf+2)/2) * (W/nf + 0.29)'
+ nrd='0.29 / W' nrs='0.29 / W' sa=0 sb=0 sd=0 mult=6 m=6
XR12 OutP VP VN sky130_fd_pr__res_high_po_1p41 L=4 mult=22 m=22
XR13 OutN VP VN sky130_fd_pr__res_high_po_1p41 L=4 mult=22 m=22
XR1 V_da2_P VP VN sky130_fd_pr__res_xhigh_po_1p41 L=2 mult=2*4 m=2*4
XR15 V_da2_N VP VN sky130_fd_pr__res_xhigh_po_1p41 L=2 mult=2*4 m=2*4
XC6 VN InputRef sky130_fd_pr__cap_mim_m3_1 W=10 L=6 MF=1 m=1
XC2 VN VP sky130_fd_pr__cap_mim_m3_1 W=15 L=30 MF=1 m=1
XC4 VN VP sky130_fd_pr__cap_mim_m3_1 W=15 L=30 MF=1 m=1
XC3 VN net2 sky130_fd_pr__cap_mim_m3_1 W=10 L=16 MF=1 m=1
.ends

.GLOBAL GND
.GLOBAL VDD
.end
